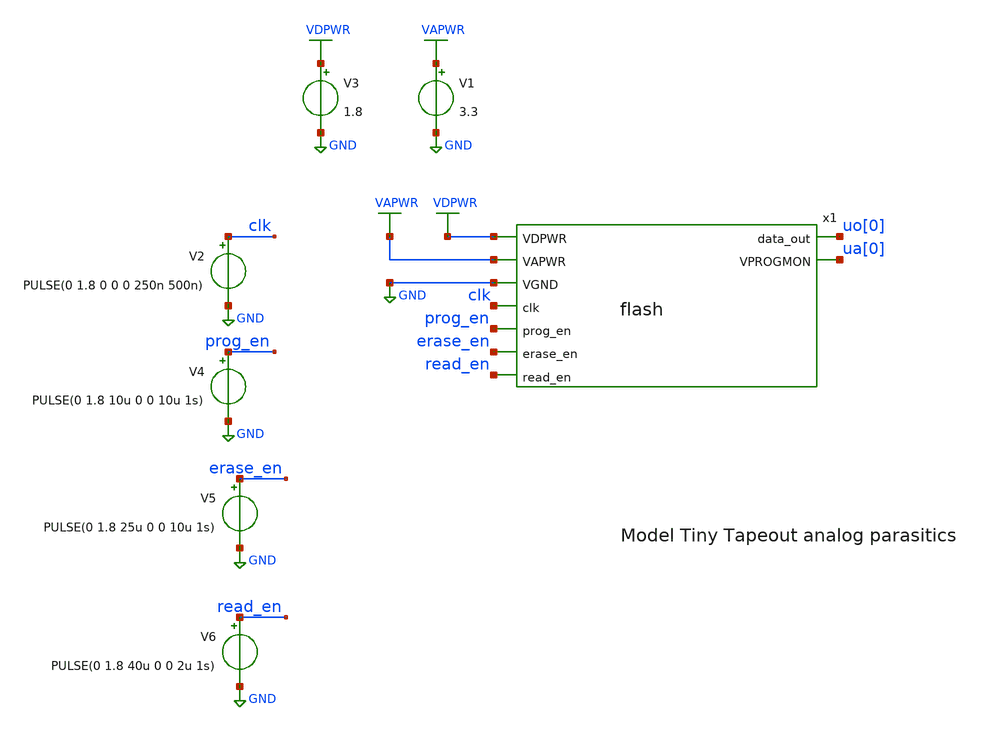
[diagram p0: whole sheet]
** sch_path: xschem/flash_tb.sch
**.subckt flash_tb
V1 VAPWR GND 3.3
V2 clk GND PULSE(0 1.8 0 0 0 250n 500n)
x1 VDPWR VAPWR GND clk prog_en erase_en read_en uo[0] ua[0] flash
V3 VDPWR GND 1.8
V4 prog_en GND PULSE(0 1.8 10u 0 0 10u 1s)
V5 erase_en GND PULSE(0 1.8 25u 0 0 10u 1s)
V6 read_en GND PULSE(0 1.8 40u 0 0 2u 1s)
**** begin user architecture code

** opencircuitdesign pdks install
.lib $::SKYWATER_MODELS/sky130.lib.spice tt
.include $::SKYWATER_MODELS/sonos_see/begin_of_life.spice





.tran 10n 100u
.save all

.control
run
write flash_tb.raw
.endc


**** end user architecture code
**.ends

* expanding   symbol:  flash.sym # of pins=9
** sym_path: xschem/flash.sym
.include ../spice/flash/lvs/flash.spice
.GLOBAL GND
.GLOBAL VAPWR
.GLOBAL VDPWR
.end
